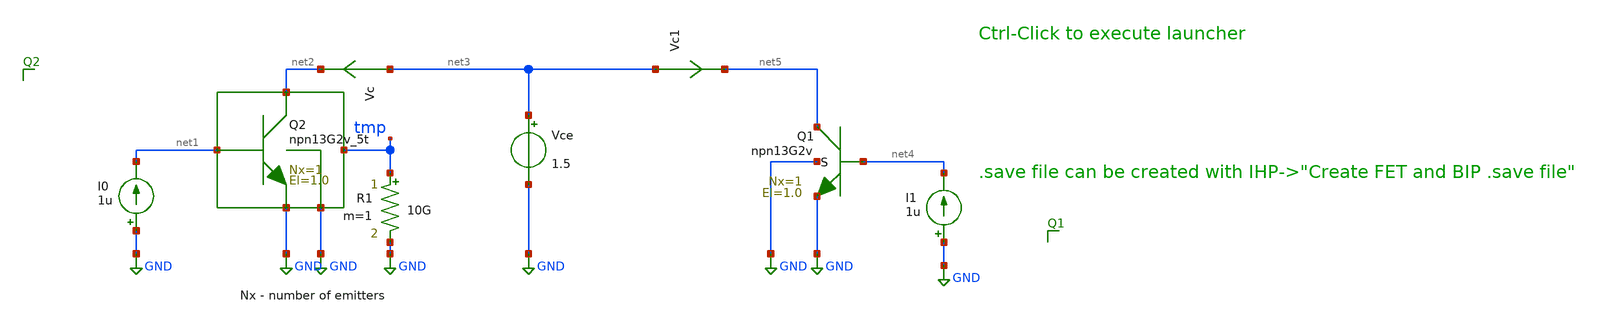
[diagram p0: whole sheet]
** sch_path: ihp-sg13g2/xschem_libs/sg13g2_tests_ase/dc_hbt_13g2v_5t/schematic/dc_hbt_13g2v_5t.sch
* Copyright 2023 IHP PDK Authors
**.subckt dc_hbt_13g2v_5t
Vce net3 GND 1.5
I0 GND net1 1u
Vc net3 net2 0
.save i(vc)
R1 tmp GND 10G m=1
I1 GND net4 1u
Vc1 net3 net5 0
.save i(vc1)
XQ1 net5 net4 GND GND npn13G2v Nx=1 El=1.0 mm_ok=1
XQ2 net2 net1 GND GND tmp npn13G2v_5t Nx=1 El=1.0 mm_ok=1
**.ends
.GLOBAL GND
.end
